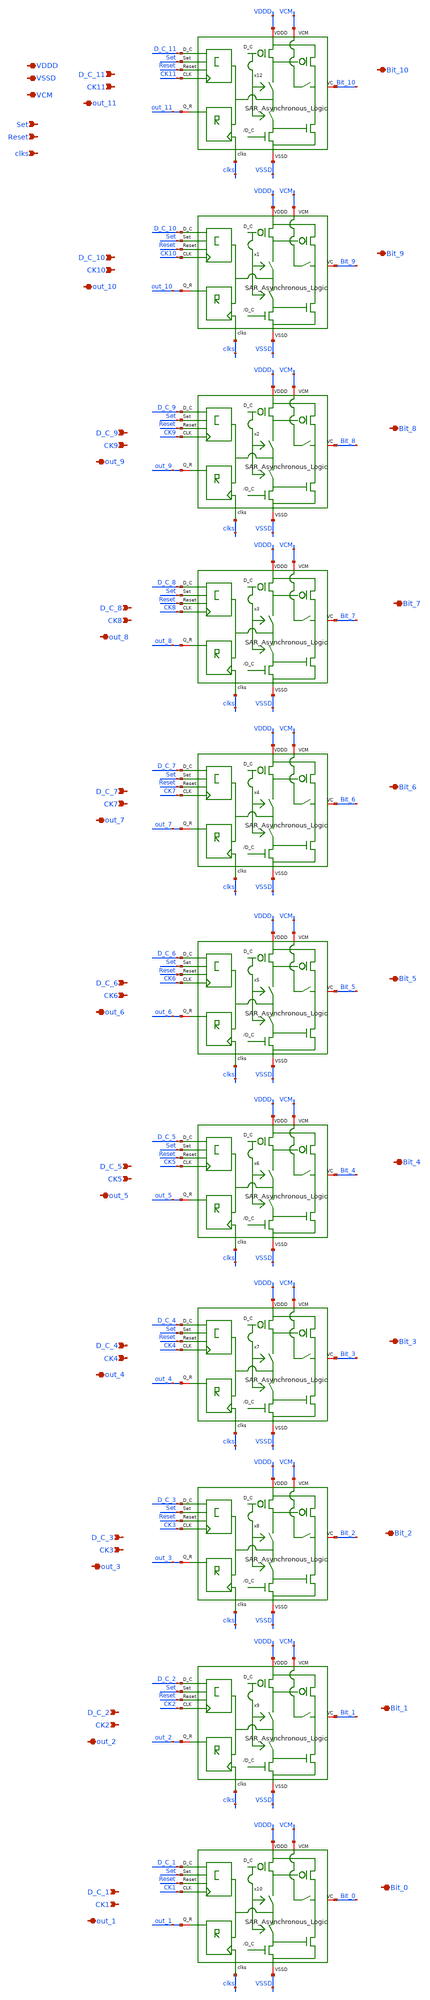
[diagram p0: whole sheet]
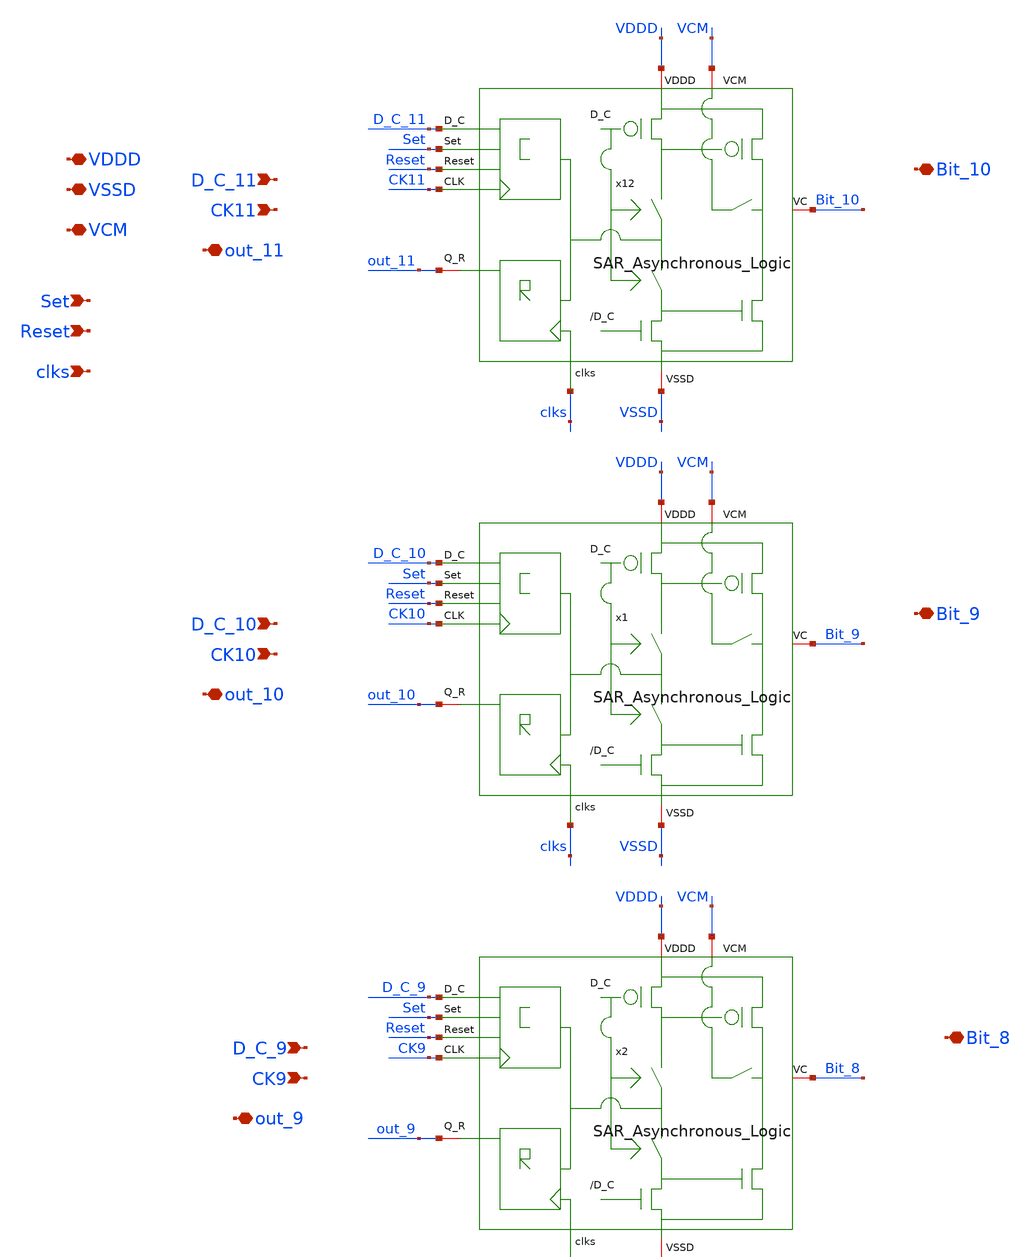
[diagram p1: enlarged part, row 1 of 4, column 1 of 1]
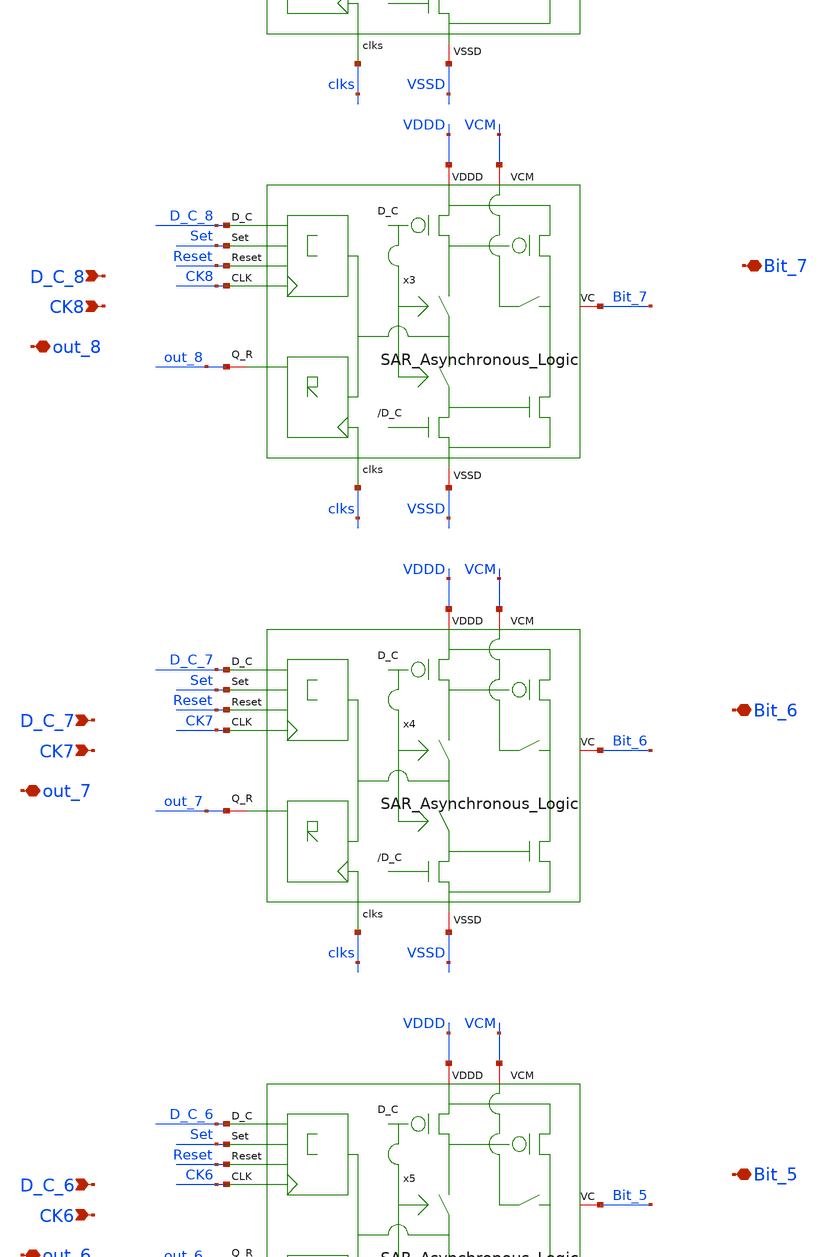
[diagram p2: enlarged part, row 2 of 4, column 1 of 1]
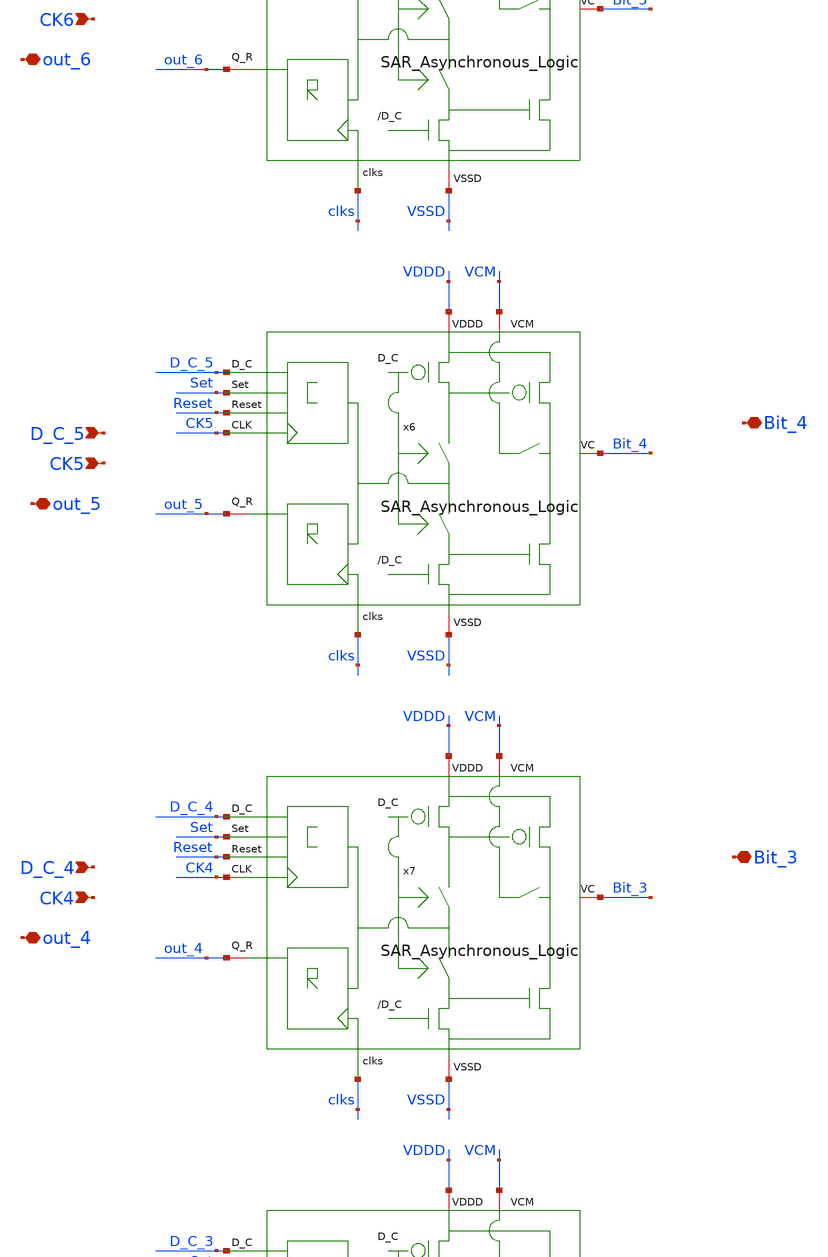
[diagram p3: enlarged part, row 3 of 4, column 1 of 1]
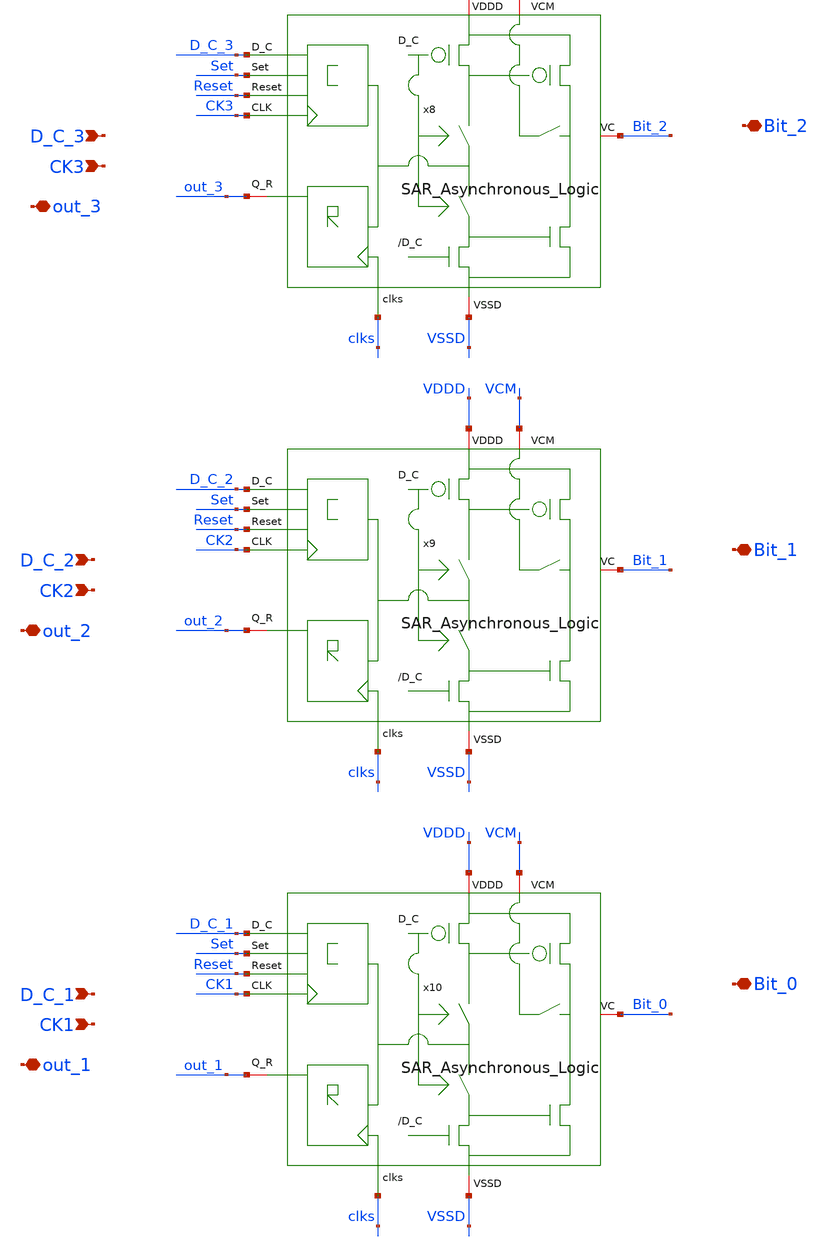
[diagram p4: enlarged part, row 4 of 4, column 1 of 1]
** sch_path: SAR_ADC/SAR_Asynchronous_Logic_integration/SAR_Asynchronous_Logic_integration.sch
**.subckt SAR_Asynchronous_Logic_integration VDDD VSSD Set Reset VCM Bit_10 clks D_C_11 CK11 out_11
*+ Bit_9 D_C_10 CK10 out_10 Bit_8 D_C_9 CK9 out_9 Bit_7 D_C_8 CK8 out_8 Bit_6 D_C_7 CK7 out_7 Bit_5 D_C_6
*+ CK6 out_6 Bit_4 D_C_5 CK5 out_5 Bit_3 D_C_4 CK4 out_4 Bit_2 D_C_3 CK3 out_3 Bit_1 D_C_2 CK2 out_2 Bit_0
*+ D_C_1 CK1 out_1
*.iopin VDDD
*.iopin VSSD
*.ipin Set
*.ipin Reset
*.iopin VCM
*.iopin Bit_10
*.ipin clks
*.ipin D_C_11
*.ipin CK11
*.iopin out_11
*.iopin Bit_9
*.ipin D_C_10
*.ipin CK10
*.iopin out_10
*.iopin Bit_8
*.ipin D_C_9
*.ipin CK9
*.iopin out_9
*.iopin Bit_7
*.ipin D_C_8
*.ipin CK8
*.iopin out_8
*.iopin Bit_6
*.ipin D_C_7
*.ipin CK7
*.iopin out_7
*.iopin Bit_5
*.ipin D_C_6
*.ipin CK6
*.iopin out_6
*.iopin Bit_4
*.ipin D_C_5
*.ipin CK5
*.iopin out_5
*.iopin Bit_3
*.ipin D_C_4
*.ipin CK4
*.iopin out_4
*.iopin Bit_2
*.ipin D_C_3
*.ipin CK3
*.iopin out_3
*.iopin Bit_1
*.ipin D_C_2
*.ipin CK2
*.iopin out_2
*.iopin Bit_0
*.ipin D_C_1
*.ipin CK1
*.iopin out_1
x12 VCM Bit_10 out_11 clks VDDD VSSD Set Reset D_C_11 CK11 SAR_Asynchronous_Logic
x1 VCM Bit_9 out_10 clks VDDD VSSD Set Reset D_C_10 CK10 SAR_Asynchronous_Logic
x2 VCM Bit_8 out_9 clks VDDD VSSD Set Reset D_C_9 CK9 SAR_Asynchronous_Logic
x3 VCM Bit_7 out_8 clks VDDD VSSD Set Reset D_C_8 CK8 SAR_Asynchronous_Logic
x4 VCM Bit_6 out_7 clks VDDD VSSD Set Reset D_C_7 CK7 SAR_Asynchronous_Logic
x5 VCM Bit_5 out_6 clks VDDD VSSD Set Reset D_C_6 CK6 SAR_Asynchronous_Logic
x6 VCM Bit_4 out_5 clks VDDD VSSD Set Reset D_C_5 CK5 SAR_Asynchronous_Logic
x7 VCM Bit_3 out_4 clks VDDD VSSD Set Reset D_C_4 CK4 SAR_Asynchronous_Logic
x8 VCM Bit_2 out_3 clks VDDD VSSD Set Reset D_C_3 CK3 SAR_Asynchronous_Logic
x9 VCM Bit_1 out_2 clks VDDD VSSD Set Reset D_C_2 CK2 SAR_Asynchronous_Logic
x10 VCM Bit_0 out_1 clks VDDD VSSD Set Reset D_C_1 CK1 SAR_Asynchronous_Logic
**.ends
.end
